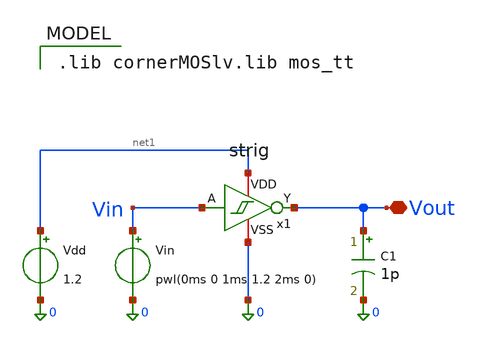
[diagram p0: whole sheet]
** sch_path: xschem/strig_tb.sch
**.subckt strig_tb Vout
*.iopin Vout
Vin Vin 0 pwl(0ms 0 1ms 1.2 2ms 0)
Vdd net1 0 1.2
C1 Vout 0 1p m=1
x1 net1 Vin Vout 0 strig WN1={WN12} WN2={WN12} WN3={WN3} WP1='2*{WN12}' WP2='2*{WN12}' WP3='2*{WN3}'
**** begin user architecture code
 .lib cornerMOSlv.lib mos_tt



.param temp=27
.param WN12=.15u
.param WN3=.15u
.option method=gear
.control
op
write strig_tb.raw
set appendwrite
foreach wn12 .15u .30u .60u .90u 1.2u 1.5u
foreach wn3 .15u .30u .60u .90u 1.2u 1.5u
  alterparam WN12 = $wn12
  alterparam WN3 = $wn3
  reset
  save all
  tran 1us 2ms
  let wn12_val = 0*time + $wn12
  let wn3_val = 0*time + $wn3
  meas tran vt_fall find v(vin) when v(vout)=0.6 fall=1
  meas tran vt_rise find v(vin) when v(vout)=0.6 rise=1
  let vth_val  = 0*time + vt_fall
  let vtl_val  = 0*time + vt_rise
  let vhys_val = vth_val - vtl_val
  write strig_tb.raw
end
end
quit 0
.endc


**** end user architecture code
**.ends

* expanding   symbol:  strig.sym # of pins=4
** sym_path: xschem/strig.sym
** sch_path: xschem/strig.sch
.subckt strig VDD A Y VSS  WN1=.15u WN2=.15u WN3=.15u WP1=.15u WP2=.15u WP3=.15u
*.iopin VDD
*.iopin VSS
*.ipin A
*.opin Y
XM1 net1 A VSS VSS sg13_lv_nmos w=WN1 l=0.13u ng=1 m=1 mm_ok=1
XM2 Y A net1 VSS sg13_lv_nmos w=WN2 l=0.13u ng=1 m=1 mm_ok=1
XM3 VDD Y net1 VSS sg13_lv_nmos w=WN3 l=0.13u ng=1 m=1 mm_ok=1
XM6 VSS Y net2 VDD sg13_lv_pmos w=WP3 l=0.13u ng=1 m=1 mm_ok=1
XM5 Y A net2 VDD sg13_lv_pmos w=WP2 l=0.13u ng=1 m=1 mm_ok=1
XM4 net2 A VDD VDD sg13_lv_pmos w=WP1 l=0.13u ng=1 m=1 mm_ok=1
.ends

.end
